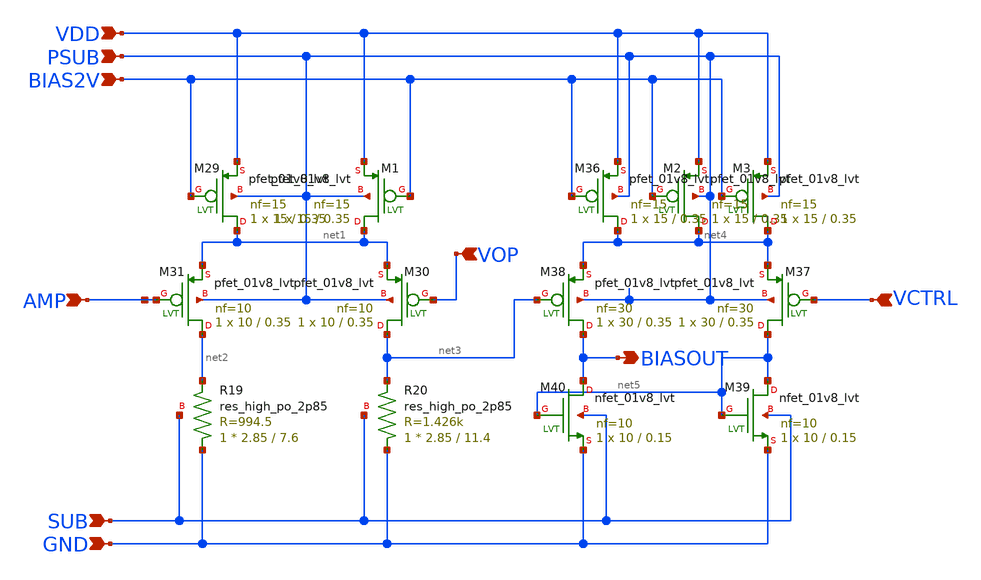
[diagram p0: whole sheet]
** sch_path: design/vco/1.7G~10G/schematic/bias_calc.sch
**.subckt bias_calc AMP VOP VCTRL BIAS2V VDD PSUB SUB GND BIASOUT
*.ipin AMP
*.ipin VOP
*.ipin VCTRL
*.ipin BIAS2V
*.ipin VDD
*.ipin PSUB
*.ipin SUB
*.ipin GND
*.opin BIASOUT
XM29 net1 BIAS2V VDD PSUB sky130_fd_pr__pfet_01v8_lvt L=0.35 W=15 nf=15 ad='int((nf+1)/2) * W/nf * 0.29'
+ as='int((nf+2)/2) * W/nf * 0.29' pd='2*int((nf+1)/2) * (W/nf + 0.29)' ps='2*int((nf+2)/2) * (W/nf + 0.29)'
+ nrd='0.29 / W' nrs='0.29 / W' sa=0 sb=0 sd=0 mult=1 m=1
XM30 net3 VOP net1 PSUB sky130_fd_pr__pfet_01v8_lvt L=0.35 W=10 nf=10 ad='int((nf+1)/2) * W/nf * 0.29'
+ as='int((nf+2)/2) * W/nf * 0.29' pd='2*int((nf+1)/2) * (W/nf + 0.29)' ps='2*int((nf+2)/2) * (W/nf + 0.29)'
+ nrd='0.29 / W' nrs='0.29 / W' sa=0 sb=0 sd=0 mult=1 m=1
XM31 net2 AMP net1 PSUB sky130_fd_pr__pfet_01v8_lvt L=0.35 W=10 nf=10 ad='int((nf+1)/2) * W/nf * 0.29'
+ as='int((nf+2)/2) * W/nf * 0.29' pd='2*int((nf+1)/2) * (W/nf + 0.29)' ps='2*int((nf+2)/2) * (W/nf + 0.29)'
+ nrd='0.29 / W' nrs='0.29 / W' sa=0 sb=0 sd=0 mult=1 m=1
XM36 net4 BIAS2V VDD PSUB sky130_fd_pr__pfet_01v8_lvt L=0.35 W=15 nf=15 ad='int((nf+1)/2) * W/nf * 0.29'
+ as='int((nf+2)/2) * W/nf * 0.29' pd='2*int((nf+1)/2) * (W/nf + 0.29)' ps='2*int((nf+2)/2) * (W/nf + 0.29)'
+ nrd='0.29 / W' nrs='0.29 / W' sa=0 sb=0 sd=0 mult=1 m=1
XM37 net5 VCTRL net4 PSUB sky130_fd_pr__pfet_01v8_lvt L=0.35 W=30 nf=30 ad='int((nf+1)/2) * W/nf * 0.29'
+ as='int((nf+2)/2) * W/nf * 0.29' pd='2*int((nf+1)/2) * (W/nf + 0.29)' ps='2*int((nf+2)/2) * (W/nf + 0.29)'
+ nrd='0.29 / W' nrs='0.29 / W' sa=0 sb=0 sd=0 mult=1 m=1
XM38 BIASOUT net3 net4 PSUB sky130_fd_pr__pfet_01v8_lvt L=0.35 W=30 nf=30 ad='int((nf+1)/2) * W/nf * 0.29'
+ as='int((nf+2)/2) * W/nf * 0.29' pd='2*int((nf+1)/2) * (W/nf + 0.29)' ps='2*int((nf+2)/2) * (W/nf + 0.29)'
+ nrd='0.29 / W' nrs='0.29 / W' sa=0 sb=0 sd=0 mult=1 m=1
XM39 net5 net5 GND SUB sky130_fd_pr__nfet_01v8_lvt L=0.15 W=10 nf=10 ad='int((nf+1)/2) * W/nf * 0.29'
+ as='int((nf+2)/2) * W/nf * 0.29' pd='2*int((nf+1)/2) * (W/nf + 0.29)' ps='2*int((nf+2)/2) * (W/nf + 0.29)'
+ nrd='0.29 / W' nrs='0.29 / W' sa=0 sb=0 sd=0 mult=1 m=1
XM40 BIASOUT net5 GND SUB sky130_fd_pr__nfet_01v8_lvt L=0.15 W=10 nf=10 ad='int((nf+1)/2) * W/nf * 0.29'
+ as='int((nf+2)/2) * W/nf * 0.29' pd='2*int((nf+1)/2) * (W/nf + 0.29)' ps='2*int((nf+2)/2) * (W/nf + 0.29)'
+ nrd='0.29 / W' nrs='0.29 / W' sa=0 sb=0 sd=0 mult=1 m=1
XR19 GND net2 SUB sky130_fd_pr__res_high_po_2p85 L=7.6 mult=1 m=1
XR20 GND net3 SUB sky130_fd_pr__res_high_po_2p85 L=11.4 mult=1 m=1
XM1 net1 BIAS2V VDD PSUB sky130_fd_pr__pfet_01v8_lvt L=0.35 W=15 nf=15 ad='int((nf+1)/2) * W/nf * 0.29'
+ as='int((nf+2)/2) * W/nf * 0.29' pd='2*int((nf+1)/2) * (W/nf + 0.29)' ps='2*int((nf+2)/2) * (W/nf + 0.29)'
+ nrd='0.29 / W' nrs='0.29 / W' sa=0 sb=0 sd=0 mult=1 m=1
XM2 net4 BIAS2V VDD PSUB sky130_fd_pr__pfet_01v8_lvt L=0.35 W=15 nf=15 ad='int((nf+1)/2) * W/nf * 0.29'
+ as='int((nf+2)/2) * W/nf * 0.29' pd='2*int((nf+1)/2) * (W/nf + 0.29)' ps='2*int((nf+2)/2) * (W/nf + 0.29)'
+ nrd='0.29 / W' nrs='0.29 / W' sa=0 sb=0 sd=0 mult=1 m=1
XM3 net4 BIAS2V VDD PSUB sky130_fd_pr__pfet_01v8_lvt L=0.35 W=15 nf=15 ad='int((nf+1)/2) * W/nf * 0.29'
+ as='int((nf+2)/2) * W/nf * 0.29' pd='2*int((nf+1)/2) * (W/nf + 0.29)' ps='2*int((nf+2)/2) * (W/nf + 0.29)'
+ nrd='0.29 / W' nrs='0.29 / W' sa=0 sb=0 sd=0 mult=1 m=1
**.ends
.end
